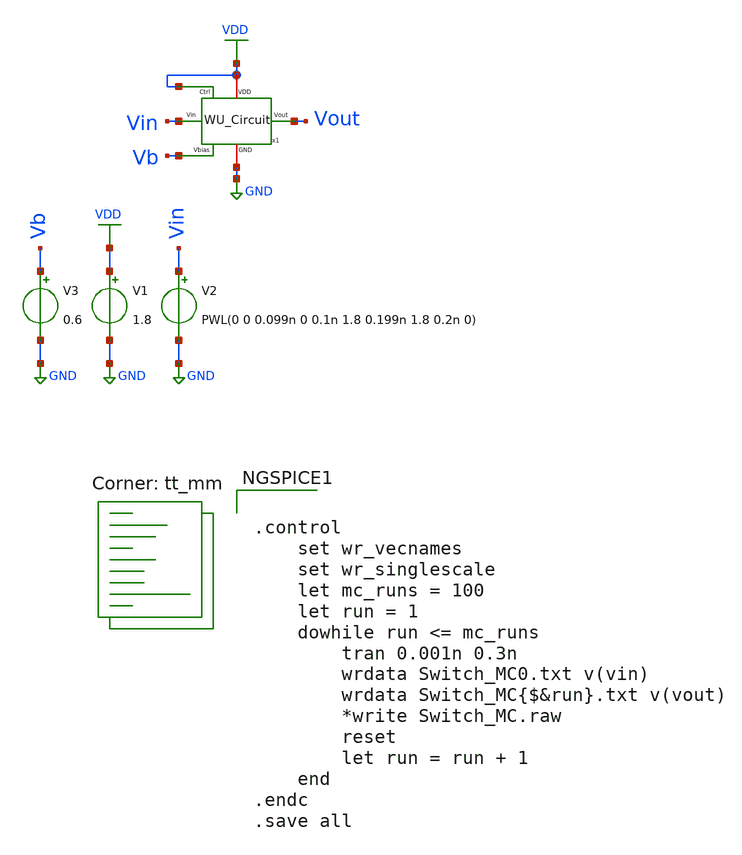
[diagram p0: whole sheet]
** sch_path: SNN/WU_Circuit_tb.sch
**.subckt WU_Circuit_tb
V1 VDD GND 1.8
V2 Vin GND PWL(0 0 0.099n 0 0.1n 1.8 0.199n 1.8 0.2n 0)
V3 Vb GND 0.6
x1 Vb VDD Vin GND VDD Vout WU_Circuit
**** begin user architecture code
.lib $::SKYWATER_MODELS/sky130.lib.spice tt_mm


.control
	set wr_vecnames
	set wr_singlescale
	let mc_runs = 100
	let run = 1
	dowhile run <= mc_runs
		tran 0.001n 0.3n
		wrdata Switch_MC0.txt v(vin)
		wrdata Switch_MC{$&run}.txt v(vout)
		*write Switch_MC.raw
		reset
		let run = run + 1
	end
.endc
.save all


**** end user architecture code
**.ends
.GLOBAL GND
.GLOBAL VDD
.end
